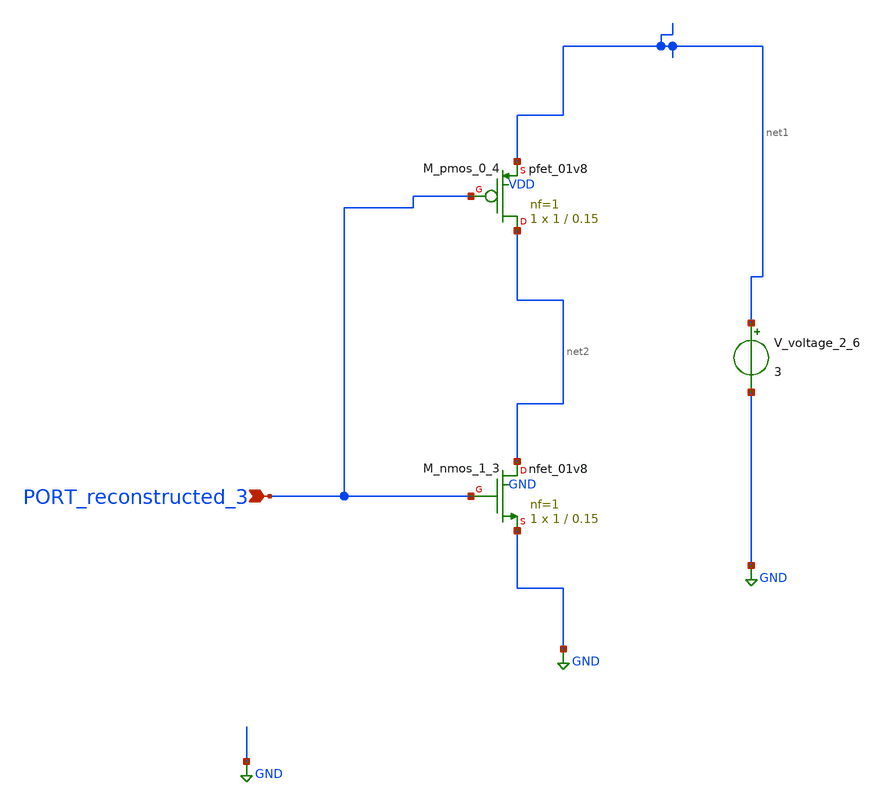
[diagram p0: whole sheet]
** sch_path: schematics/AMSNet/61.sch
**.subckt 61 PORT_reconstructed_3
*.ipin PORT_reconstructed_3
XM_nmos_1_3 net2 PORT_reconstructed_3 GND GND sky130_fd_pr__nfet_01v8 L=0.15 W=1 nf=1 ad='int((1 + 1)/2) * 1 / 1 * 0.29'
+ as='int((1 + 2)/2) * 1 / 1 * 0.29' pd='2*int((1 + 1)/2) * (1 / 1 + 0.29)' ps='2*int((1 + 2)/2) * (1 / 1 + 0.29)'
+ nrd='0.29 / 1 ' nrs='0.29 / 1 ' sa=0 sb=0 sd=0 mult=1 m=1
XM_pmos_0_4 net2 PORT_reconstructed_3 net1 VDD sky130_fd_pr__pfet_01v8 L=0.15 W=1 nf=1 ad='int((1 + 1)/2) * 1 / 1 * 0.29'
+ as='int((1 + 2)/2) * 1 / 1 * 0.29' pd='2*int((1 + 1)/2) * (1 / 1 + 0.29)' ps='2*int((1 + 2)/2) * (1 / 1 + 0.29)'
+ nrd='0.29 / 1 ' nrs='0.29 / 1 ' sa=0 sb=0 sd=0 mult=1 m=1
V_voltage_2_6 net1 GND 3
**.ends
.GLOBAL GND
.end
